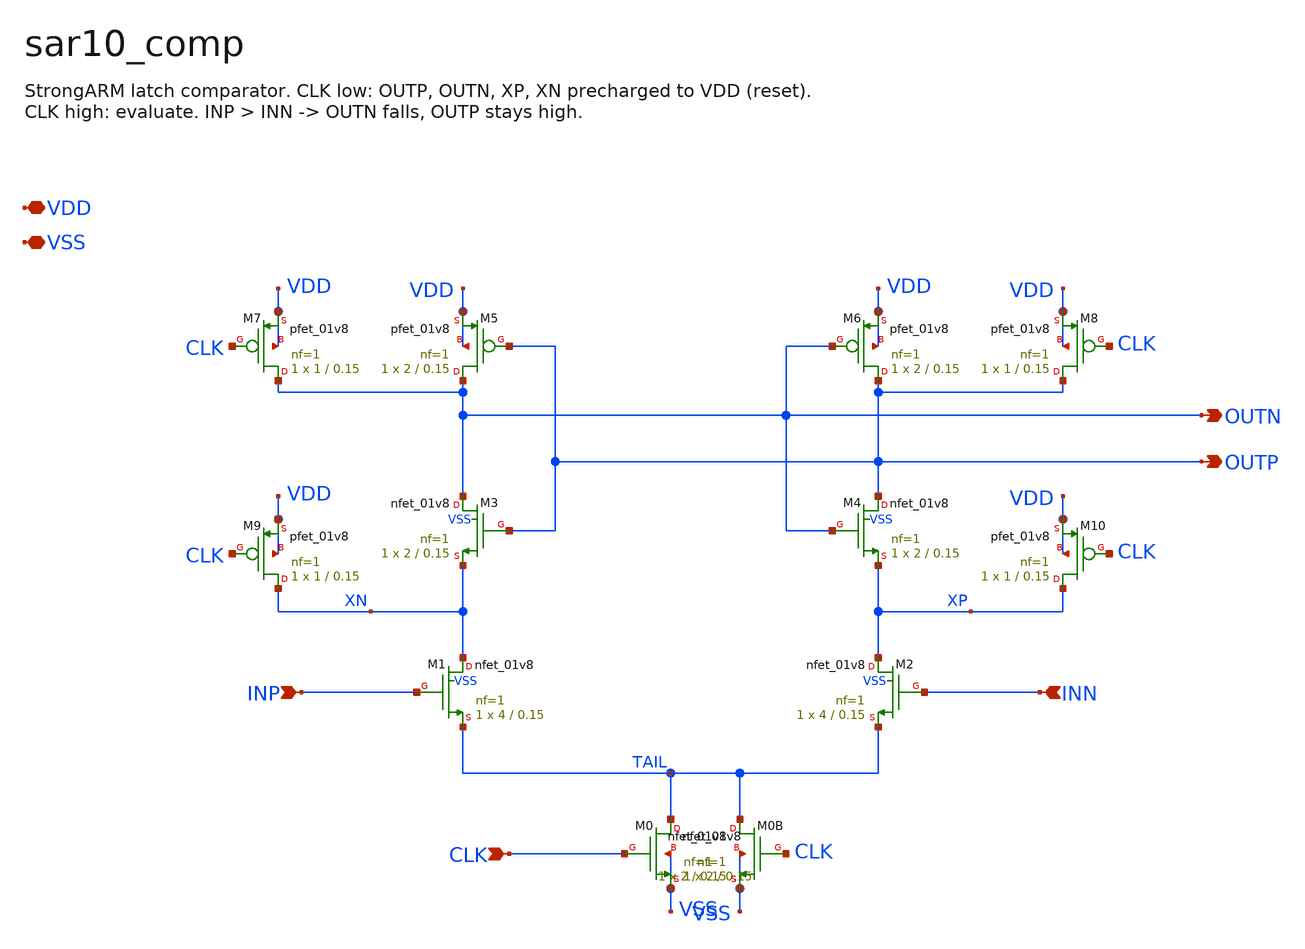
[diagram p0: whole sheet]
** sch_path: xschem/sar10_comp.sch
**.subckt sar10_comp INP INN CLK OUTP OUTN VDD VSS
*.ipin INP
*.ipin INN
*.ipin CLK
*.opin OUTP
*.opin OUTN
*.iopin VDD
*.iopin VSS
XM0 TAIL CLK VSS VSS sky130_fd_pr__nfet_01v8 L=0.15 W=2 nf=1 ad='int((1 + 1)/2) * 2 / 1 * 0.29' as='int((1 + 2)/2) * 2 / 1 * 0.29'
+ pd='2*int((1 + 1)/2) * (2 / 1 + 0.29)' ps='2*int((1 + 2)/2) * (2 / 1 + 0.29)' nrd='0.29 / 2 ' nrs='0.29 / 2 '
+ sa=0 sb=0 sd=0 mult=1 m=1
XM0B TAIL CLK VSS VSS sky130_fd_pr__nfet_01v8 L=0.15 W=2 nf=1 ad='int((1 + 1)/2) * 2 / 1 * 0.29' as='int((1 + 2)/2) * 2 / 1 * 0.29'
+ pd='2*int((1 + 1)/2) * (2 / 1 + 0.29)' ps='2*int((1 + 2)/2) * (2 / 1 + 0.29)' nrd='0.29 / 2 ' nrs='0.29 / 2 '
+ sa=0 sb=0 sd=0 mult=1 m=1
XM1 XN INP TAIL VSS sky130_fd_pr__nfet_01v8 L=0.15 W=4 nf=1 ad='int((1 + 1)/2) * 4 / 1 * 0.29' as='int((1 + 2)/2) * 4 / 1 * 0.29'
+ pd='2*int((1 + 1)/2) * (4 / 1 + 0.29)' ps='2*int((1 + 2)/2) * (4 / 1 + 0.29)' nrd='0.29 / 4 ' nrs='0.29 / 4 '
+ sa=0 sb=0 sd=0 mult=1 m=1
XM2 XP INN TAIL VSS sky130_fd_pr__nfet_01v8 L=0.15 W=4 nf=1 ad='int((1 + 1)/2) * 4 / 1 * 0.29' as='int((1 + 2)/2) * 4 / 1 * 0.29'
+ pd='2*int((1 + 1)/2) * (4 / 1 + 0.29)' ps='2*int((1 + 2)/2) * (4 / 1 + 0.29)' nrd='0.29 / 4 ' nrs='0.29 / 4 '
+ sa=0 sb=0 sd=0 mult=1 m=1
XM3 OUTN OUTP XN VSS sky130_fd_pr__nfet_01v8 L=0.15 W=2 nf=1 ad='int((1 + 1)/2) * 2 / 1 * 0.29' as='int((1 + 2)/2) * 2 / 1 * 0.29'
+ pd='2*int((1 + 1)/2) * (2 / 1 + 0.29)' ps='2*int((1 + 2)/2) * (2 / 1 + 0.29)' nrd='0.29 / 2 ' nrs='0.29 / 2 '
+ sa=0 sb=0 sd=0 mult=1 m=1
XM4 OUTP OUTN XP VSS sky130_fd_pr__nfet_01v8 L=0.15 W=2 nf=1 ad='int((1 + 1)/2) * 2 / 1 * 0.29' as='int((1 + 2)/2) * 2 / 1 * 0.29'
+ pd='2*int((1 + 1)/2) * (2 / 1 + 0.29)' ps='2*int((1 + 2)/2) * (2 / 1 + 0.29)' nrd='0.29 / 2 ' nrs='0.29 / 2 '
+ sa=0 sb=0 sd=0 mult=1 m=1
XM5 OUTN OUTP VDD VDD sky130_fd_pr__pfet_01v8 L=0.15 W=2 nf=1 ad='int((1 + 1)/2) * 2 / 1 * 0.29' as='int((1 + 2)/2) * 2 / 1 * 0.29'
+ pd='2*int((1 + 1)/2) * (2 / 1 + 0.29)' ps='2*int((1 + 2)/2) * (2 / 1 + 0.29)' nrd='0.29 / 2 ' nrs='0.29 / 2 '
+ sa=0 sb=0 sd=0 mult=1 m=1
XM6 OUTP OUTN VDD VDD sky130_fd_pr__pfet_01v8 L=0.15 W=2 nf=1 ad='int((1 + 1)/2) * 2 / 1 * 0.29' as='int((1 + 2)/2) * 2 / 1 * 0.29'
+ pd='2*int((1 + 1)/2) * (2 / 1 + 0.29)' ps='2*int((1 + 2)/2) * (2 / 1 + 0.29)' nrd='0.29 / 2 ' nrs='0.29 / 2 '
+ sa=0 sb=0 sd=0 mult=1 m=1
XM7 OUTN CLK VDD VDD sky130_fd_pr__pfet_01v8 L=0.15 W=1 nf=1 ad='int((1 + 1)/2) * 1 / 1 * 0.29' as='int((1 + 2)/2) * 1 / 1 * 0.29'
+ pd='2*int((1 + 1)/2) * (1 / 1 + 0.29)' ps='2*int((1 + 2)/2) * (1 / 1 + 0.29)' nrd='0.29 / 1 ' nrs='0.29 / 1 '
+ sa=0 sb=0 sd=0 mult=1 m=1
XM8 OUTP CLK VDD VDD sky130_fd_pr__pfet_01v8 L=0.15 W=1 nf=1 ad='int((1 + 1)/2) * 1 / 1 * 0.29' as='int((1 + 2)/2) * 1 / 1 * 0.29'
+ pd='2*int((1 + 1)/2) * (1 / 1 + 0.29)' ps='2*int((1 + 2)/2) * (1 / 1 + 0.29)' nrd='0.29 / 1 ' nrs='0.29 / 1 '
+ sa=0 sb=0 sd=0 mult=1 m=1
XM9 XN CLK VDD VDD sky130_fd_pr__pfet_01v8 L=0.15 W=1 nf=1 ad='int((1 + 1)/2) * 1 / 1 * 0.29' as='int((1 + 2)/2) * 1 / 1 * 0.29'
+ pd='2*int((1 + 1)/2) * (1 / 1 + 0.29)' ps='2*int((1 + 2)/2) * (1 / 1 + 0.29)' nrd='0.29 / 1 ' nrs='0.29 / 1 '
+ sa=0 sb=0 sd=0 mult=1 m=1
XM10 XP CLK VDD VDD sky130_fd_pr__pfet_01v8 L=0.15 W=1 nf=1 ad='int((1 + 1)/2) * 1 / 1 * 0.29' as='int((1 + 2)/2) * 1 / 1 * 0.29'
+ pd='2*int((1 + 1)/2) * (1 / 1 + 0.29)' ps='2*int((1 + 2)/2) * (1 / 1 + 0.29)' nrd='0.29 / 1 ' nrs='0.29 / 1 '
+ sa=0 sb=0 sd=0 mult=1 m=1
**.ends
.end
